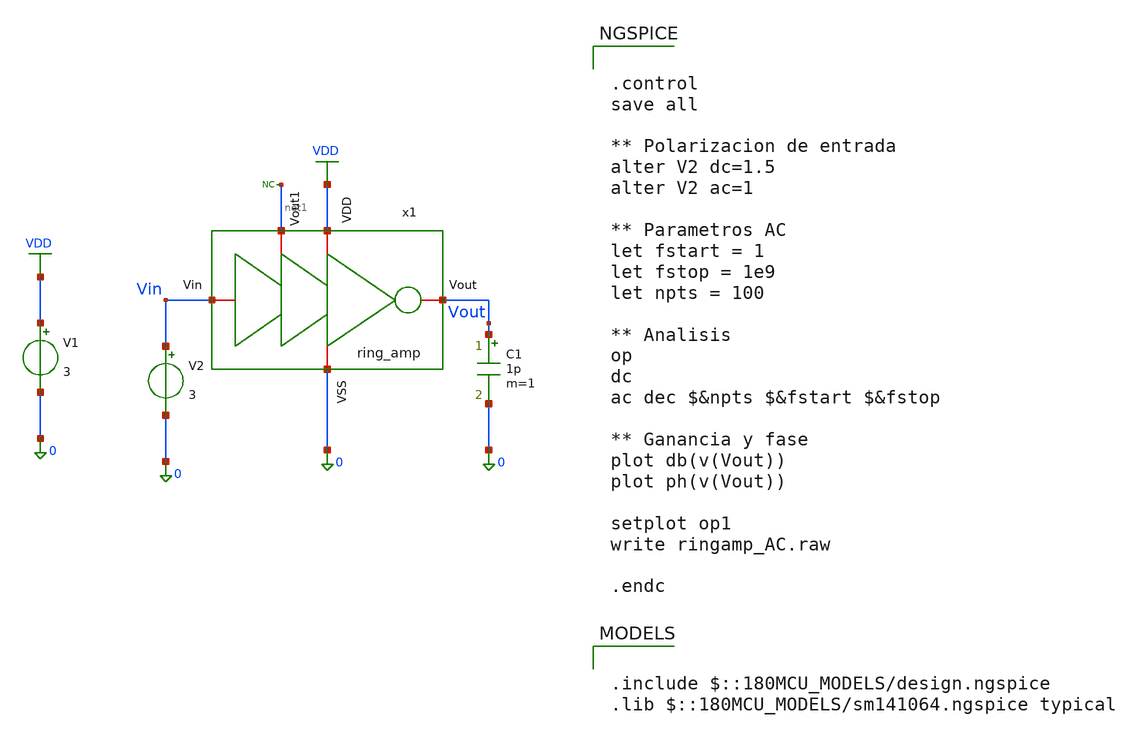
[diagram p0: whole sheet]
** sch_path: designs/DS_modulator/ring_amp/xschem/ring_amp_TB_AC.sch
**.subckt ring_amp_TB_AC
x1 VDD Vin Vout net1 0 ring_amp
C1 Vout 0 1p m=1
* noconn #net1
V1 VDD 0 3
V2 Vin 0 3
**** begin user architecture code

.include $::180MCU_MODELS/design.ngspice
.lib $::180MCU_MODELS/sm141064.ngspice typical



.control
save all

** Polarizacion de entrada
alter V2 dc=1.5
alter V2 ac=1

** Parametros AC
let fstart = 1
let fstop = 1e9
let npts = 100

** Analisis
op
dc
ac dec $&npts $&fstart $&fstop

** Ganancia y fase
plot db(v(Vout))
plot ph(v(Vout))

setplot op1
write ringamp_AC.raw

.endc


**** end user architecture code
**.ends
.GLOBAL VDD
.end
